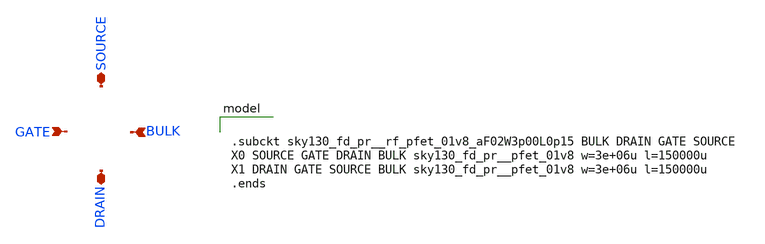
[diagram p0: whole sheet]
** sch_path: xschem/sky130_fd_pr__rf_pfet_01v8_aF02W3p00L0p15.sch
**.subckt sky130_fd_pr__rf_pfet_01v8_aF02W3p00L0p15 SOURCE DRAIN BULK GATE
*.iopin SOURCE
*.iopin DRAIN
*.ipin BULK
*.ipin GATE
**** begin user architecture code


.subckt sky130_fd_pr__rf_pfet_01v8_aF02W3p00L0p15 BULK DRAIN GATE SOURCE
X0 SOURCE GATE DRAIN BULK sky130_fd_pr__pfet_01v8 w=3e+06u l=150000u
X1 DRAIN GATE SOURCE BULK sky130_fd_pr__pfet_01v8 w=3e+06u l=150000u
.ends

**** end user architecture code
**.ends
.end
